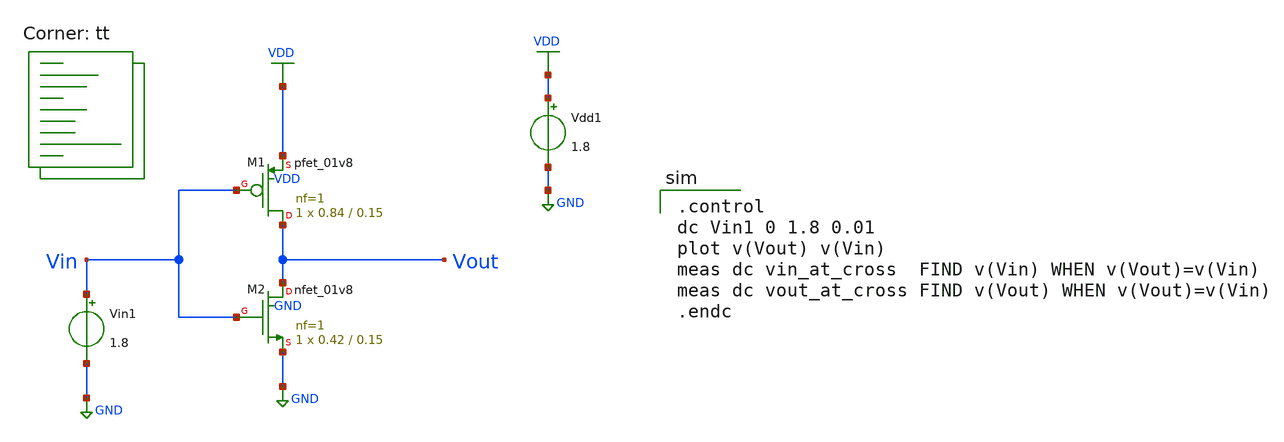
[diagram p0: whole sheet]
** sch_path: tutorial-2/source/q1_vtc.sch
**.subckt q1_vtc
XM1 Vout Vin VDD VDD sky130_fd_pr__pfet_01v8 L=0.15 W=0.84 nf=1 ad='int((nf+1)/2) * W/nf * 0.29' as='int((nf+2)/2) * W/nf * 0.29'
+ pd='2*int((nf+1)/2) * (W/nf + 0.29)' ps='2*int((nf+2)/2) * (W/nf + 0.29)' nrd='0.29 / W' nrs='0.29 / W'
+ sa=0 sb=0 sd=0 mult=1 m=1
XM2 Vout Vin GND GND sky130_fd_pr__nfet_01v8 L=0.15 W=0.42 nf=1 ad='int((nf+1)/2) * W/nf * 0.29' as='int((nf+2)/2) * W/nf * 0.29'
+ pd='2*int((nf+1)/2) * (W/nf + 0.29)' ps='2*int((nf+2)/2) * (W/nf + 0.29)' nrd='0.29 / W' nrs='0.29 / W'
+ sa=0 sb=0 sd=0 mult=1 m=1
Vdd1 VDD GND 1.8
Vin1 Vin GND 1.8
**** begin user architecture code
.lib $::SKYWATER_MODELS/sky130.lib.spice tt

.control
dc Vin1 0 1.8 0.01
plot v(Vout) v(Vin)
meas dc vin_at_cross  FIND v(Vin) WHEN v(Vout)=v(Vin)
meas dc vout_at_cross FIND v(Vout) WHEN v(Vout)=v(Vin)
.endc

**** end user architecture code
**.ends
.GLOBAL VDD
.GLOBAL GND
.end
